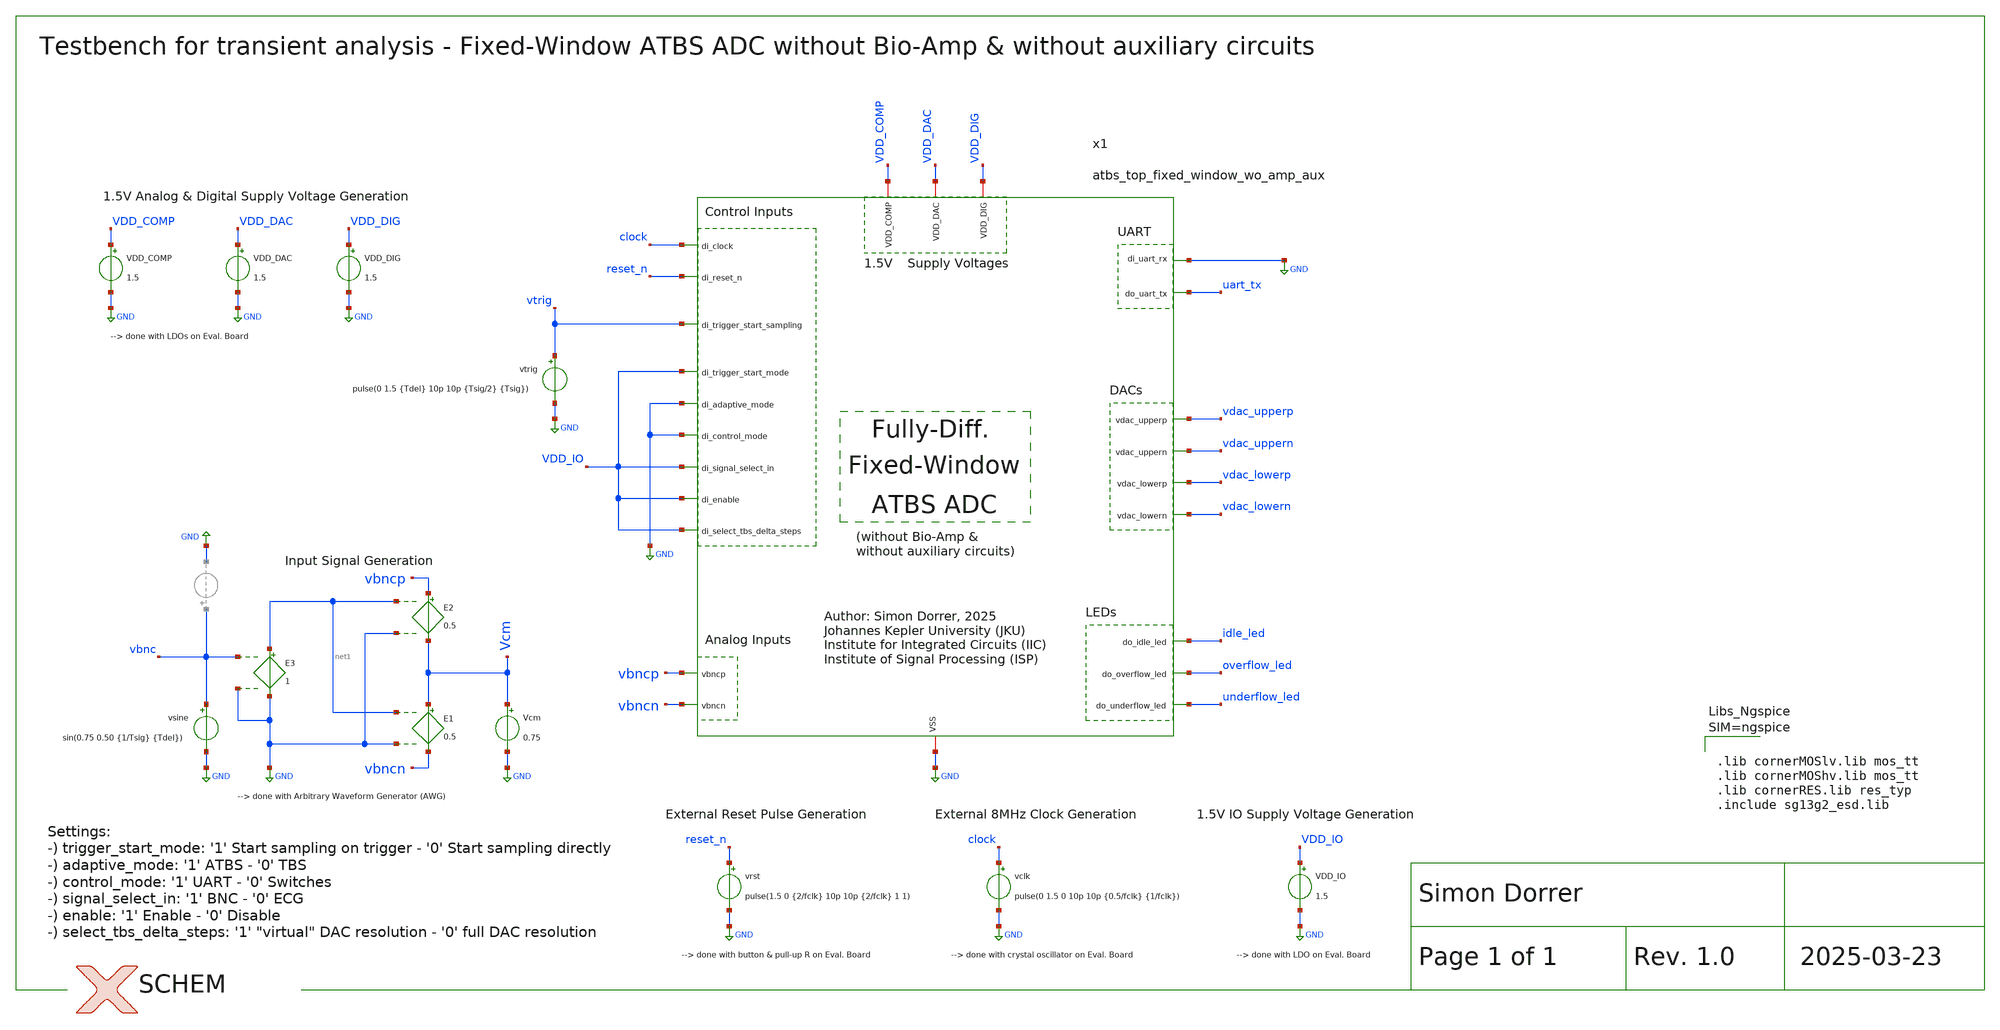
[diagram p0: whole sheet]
** sch_path: SG13G2_ATBS-ADC-main/xschem/top_level/testbenches/atbs_top_fixed_window_wo_amp_aux_tb_tran.sch
**.subckt atbs_top_fixed_window_wo_amp_aux_tb_tran
VDD_DAC VDD_DAC GND 1.5
VDD_COMP VDD_COMP GND 1.5
VDD_DIG VDD_DIG GND 1.5
VDD_IO VDD_IO GND 1.5
Vcm Vcm GND 0.75
E1 Vcm vbncn net1 GND 0.5
E2 vbncp Vcm net1 GND 0.5
E3 net1 GND vbnc GND 1
vsine vbnc GND sin(0.75 0.50 {1/Tsig} {Tdel})
vtrig vtrig GND pulse(0 1.5 {Tdel} 10p 10p {Tsig/2} {Tsig})
vrst reset_n GND pulse(1.5 0 {2/fclk} 10p 10p {2/fclk} 1 1)
vclk clock GND pulse(0 1.5 0 10p 10p {0.5/fclk} {1/fclk})
x1 VDD_DIG VDD_COMP clock reset_n vtrig VDD_DAC VDD_IO GND GND VDD_IO VDD_IO VDD_IO GND uart_tx
+ idle_led overflow_led underflow_led GND vbncp vbncn vdac_uppern vdac_lowern vdac_upperp vdac_lowerp
+ atbs_top_fixed_window_wo_amp_aux
**** begin user architecture code



* Gate-Level Analog Mixed Signal Simulation (.xspice)
.include /foss/designs/SG13G2_ATBS-ADC-main/xspice/atbs_core_fixed_window_board/atbs_core_fixed_window_board.xspice
.param temp=27
.param fclk=8000000
.csparam fclk=fclk
*.param Tsig=20m
*.param Tdel=20m
.param Tsig=200u
.param Tdel=100u
.csparam Tdel=Tdel
.csparam Tsig=Tsig
.options savecurrents method=gear reltol=1e-2 abstol=1e-12 gmin=1e-12 rshunt=1e12
.control

optran 0 0 0 1u 1m 0

* save all
save vbnc vbncp vbncn vtrig clock reset_n uart_tx idle_led overflow_led underflow_led vdac_upperp
+ vdac_uppern vdac_lowerp vdac_lowern
save x1.Vcm
save x1.spike x1.bio_amp_en x1.en_cap_1 x1.en_cap_2 x1.en_cap_3 x1.spdt_ctrl
save x1.phi_vcm_generator_1 x1.phi_vcm_generator_2 x1.phi_bias_1 x1.phi_bias_2 x1.phi_cmfb_1
+ x1.phi_cmfb_2 x1.phi_R_1 x1.phi_R_2
save x1.phi_comp x1.vcomp_upper x1.vcomp_lower x1.phi_dac_upper x1.dac_D0_upper x1.dac_D1_upper
+ x1.dac_D2_upper x1.dac_D3_upper x1.phi_dac_lower x1.dac_D0_lower x1.dac_D1_lower x1.dac_D2_lower x1.dac_D3_lower

* Transient Analysis
let tstep = 1/fclk
let tstop = Tdel + 4*Tsig
tran $&tstep $&tstop
write atbs_top_fixed_window_wo_amp_aux_tb_tran.raw

* Plotting Data
let vdac_upper = vdac_upperp - vdac_uppern
let vdac_lower = vdac_lowerp - vdac_lowern
plot v(vbnc) v(vtrig) v(vdac_upper) v(vdac_lower)

* Calculate Energy / Conversion (ToDo for all VDDs and add together in the end)
* i_int in As
* energy_conv in Ws = J
* let N = 1
* let t_conv = 1/fclk
* meas tran i_int INTEG i(VDD) from=0p to=t_conv
* let energy_conv = 1.5 * i_int / N

* let energy_conv_pico = energy_conv * 1e12
* echo Energy / Conversion $&energy_conv_pico pJ/conv

* Calculate Power Consumption (ToDo)
* let power = energy_conv / t_conv * 1e6
* echo Power Consumption $&power uW

* Writing Data
set wr_singlescale
set wr_vecnames
wrdata
+ /foss/designs/SG13G2_ATBS-ADC-main/python/plot_simulations/data/atbs_top_fixed_window_wo_amp_aux_tb_tran.txt v(vbnc) v(vtrig) v(vdac_upper) v(vdac_lower)

let uart_tx = uart_tx
wrdata
+ /foss/designs/SG13G2_ATBS-ADC-main/python/reconstruction/data/atbs_top_fixed_window_wo_amp_aux_tb_tran_uart.txt v(clock) v(uart_tx)
set appendwrite

.endc





.lib cornerMOSlv.lib mos_tt
.lib cornerMOShv.lib mos_tt
.lib cornerRES.lib res_typ
.include sg13g2_esd.lib



**** end user architecture code
**.ends

* expanding   symbol:  top_level/atbs_top_fixed_window_wo_amp_aux.sym # of pins=24
** sym_path: SG13G2_ATBS-ADC-main/xschem/top_level/atbs_top_fixed_window_wo_amp_aux.sym
** sch_path: SG13G2_ATBS-ADC-main/xschem/top_level/atbs_top_fixed_window_wo_amp_aux.sch
.subckt atbs_top_fixed_window_wo_amp_aux VDD_DIG VDD_COMP di_clock di_reset_n
+ di_trigger_start_sampling VDD_DAC di_trigger_start_mode di_adaptive_mode di_control_mode di_signal_select_in di_enable
+ di_select_tbs_delta_steps di_uart_rx do_uart_tx do_idle_led do_overflow_led do_underflow_led VSS vbncp vbncn vdac_uppern
+ vdac_lowern vdac_upperp vdac_lowerp
*.iopin VDD_DIG
*.iopin VDD_COMP
*.iopin VSS
*.ipin di_clock
*.ipin di_reset_n
*.iopin VDD_DAC
*.ipin di_uart_rx
*.opin do_uart_tx
*.ipin di_trigger_start_sampling
*.ipin di_trigger_start_mode
*.ipin di_adaptive_mode
*.ipin di_control_mode
*.ipin di_signal_select_in
*.ipin di_enable
*.ipin di_select_tbs_delta_steps
*.opin do_idle_led
*.opin do_overflow_led
*.opin do_underflow_led
*.ipin vbncp
*.ipin vbncn
*.opin vdac_upperp
*.opin vdac_lowern
*.opin vdac_uppern
*.opin vdac_lowerp
x4 VDD_COMP vdac_upperp vcomp_upper vdac_uppern phi_comp VSS DT_comparator
x5 VDD_COMP vdac_lowerp vcomp_lower vdac_lowern phi_comp VSS DT_comparator
x30 VDD_DIG VSS di_adaptive_mode bio_amp_en di_clock vcomp_lower vcomp_upper di_control_mode
+ dac_D0_lower dac_D1_lower dac_D2_lower dac_D3_lower dac_D0_upper dac_D1_upper dac_D2_upper dac_D3_upper
+ di_enable do_idle_led do_overflow_led phi_bias_1 phi_bias_2 phi_cmfb_1 phi_cmfb_2 phi_comp phi_dac_lower
+ phi_dac_upper phi_R_1 phi_R_2 phi_vcm_generator_1 phi_vcm_generator_2 di_reset_n en_cap_1 en_cap_2 en_cap_3
+ spdt_ctrl di_select_tbs_delta_steps di_signal_select_in spike di_trigger_start_mode di_trigger_start_sampling
+ di_uart_rx do_uart_tx do_underflow_led atbs_core_fixed_window_board
x32 VDD_DIG phi_vcm_generator_2 phi_vcm_generator_1 Vcm VSS vcm_generator C_VCM=1p W_P_VCM=1.0u
+ L_P_VCM=0.13u W_N_VCM=1.0u L_N_VCM=0.13u
x31 VDD_DAC vbncp vdac_upperp vdac_uppern vbncn dac_D0_lower dac_D1_lower dac_D2_lower dac_D3_lower
+ VSS VDD_DAC Vcm vdac_lowerp vdac_lowern phi_dac_lower dac_D0_upper dac_D1_upper dac_D2_upper
+ dac_D3_upper phi_dac_upper dac W_P_SPDT=1.0u L_P_SPDT=0.13u W_N_SPDT=1.0u L_N_SPDT=0.13u C2=1024f Cu=8f
+ Cucomp=8.1f
.ends


* expanding   symbol:  comparator/discrete_time/DT_comparator.sym # of pins=6
** sym_path: SG13G2_ATBS-ADC-main/xschem/comparator/discrete_time/DT_comparator.sym
** sch_path: SG13G2_ATBS-ADC-main/xschem/comparator/discrete_time/DT_comparator.sch
.subckt DT_comparator VDD vinp vout vinn di_clk VSS
*.iopin VDD
*.opin vout
*.iopin VSS
*.ipin vinp
*.ipin vinn
*.ipin di_clk
x2 VDD voutp_comp voutp_buf VSS buffer_lv W_P_INV=1.0u L_P_INV=0.13u W_N_INV=1.0u L_N_INV=0.13u
x3 VDD voutn_comp voutn_buf VSS buffer_lv W_P_INV=1.0u L_P_INV=0.13u W_N_INV=1.0u L_N_INV=0.13u
x5 VDD di_clk net1 VSS inverter_lv W_P=1.0u L_P=0.13u W_N=1.0u L_N=0.13u
* noconn #net2
x4 VDD voutp_buf net2 VSS vout voutn_buf SR_latch W_P_SR=1.0u L_P_SR=0.13u W_N_SR=1.0u L_N_SR=0.13u
x1 net1 di_clk VDD voutp_comp vinp VSS voutn_comp vinn dynamic_biasing_comparator
.ends


* expanding   symbol:  vcm_generator/vcm_generator.sym # of pins=5
** sym_path: SG13G2_ATBS-ADC-main/xschem/vcm_generator/vcm_generator.sym
** sch_path: SG13G2_ATBS-ADC-main/xschem/vcm_generator/vcm_generator.sch
.subckt vcm_generator VDD di_phi_2 di_phi_1 Vcm VSS  C_VCM=1p W_P_VCM=1.0u L_P_VCM=0.13u
+ W_N_VCM=1.0u L_N_VCM=0.13u
*.iopin VDD
*.opin Vcm
*.iopin VSS
*.ipin di_phi_1
*.ipin di_phi_2
x1 VDD di_phi_2 VSS net1 VDD di_phi_2_n transmission_gate_lv_wo_dummy W_P=W_P_VCM L_P=L_P_VCM
+ W_N=W_N_VCM L_N=L_N_VCM
x2 VDD di_phi_1 VSS Vcm net1 di_phi_1_n transmission_gate_lv_wo_dummy W_P=W_P_VCM L_P=L_P_VCM
+ W_N=W_N_VCM L_N=L_N_VCM
x3 VDD di_phi_2 VSS net3 net2 di_phi_2_n transmission_gate_lv_wo_dummy W_P=W_P_VCM L_P=L_P_VCM
+ W_N=W_N_VCM L_N=L_N_VCM
x4 VDD di_phi_1 VSS Vcm net3 di_phi_1_n transmission_gate_lv_wo_dummy W_P=W_P_VCM L_P=L_P_VCM
+ W_N=W_N_VCM L_N=L_N_VCM
x5 VDD di_phi_1 VSS VSS net2 di_phi_1_n transmission_gate_lv_wo_dummy W_P=W_P_VCM L_P=L_P_VCM
+ W_N=W_N_VCM L_N=L_N_VCM
x9 VDD di_phi_1 di_phi_1_n VSS inverter_lv W_P=W_P_VCM L_P=L_P_VCM W_N=W_N_VCM L_N=L_N_VCM
x8 VDD di_phi_2 di_phi_2_n VSS inverter_lv W_P=W_P_VCM L_P=L_P_VCM W_N=W_N_VCM L_N=L_N_VCM
C1 net1 net2 C_VCM m=1
C2 net3 VSS C_VCM m=1
.ends


* expanding   symbol:  dac/dac.sym # of pins=20
** sym_path: SG13G2_ATBS-ADC-main/xschem/dac/dac.sym
** sch_path: SG13G2_ATBS-ADC-main/xschem/dac/dac.sch
.subckt dac VDD vinp voutp1 voutn1 vinn di_D0_2 di_D1_2 di_D2_2 di_D3_2 VSS Vref Vcm voutp2 voutn2
+ di_clk_2 di_D0_1 di_D1_1 di_D2_1 di_D3_1 di_clk_1  W_P_SPDT=1.0u L_P_SPDT=0.13u W_N_SPDT=1.0u L_N_SPDT=0.13u
+ C2=1024f Cu=8f Cucomp=8.1f
*.opin voutp1
*.ipin di_D0_1
*.iopin VSS
*.iopin Vref
*.opin voutn1
*.ipin vinp
*.ipin vinn
*.ipin di_D1_1
*.ipin di_D2_1
*.ipin di_D3_1
*.opin voutp2
*.opin voutn2
*.iopin VDD
*.ipin Vcm
*.ipin di_clk_1
*.ipin di_D3_2
*.ipin di_D2_2
*.ipin di_D1_2
*.ipin di_D0_2
*.ipin di_clk_2
C2a vinp voutp1 C2 m=1
C2b vinn voutn1 C2 m=1
C1a net3 voutp1 Cucomp m=1
C1b net1 voutn1 Cucomp m=1
x2 VDD di_clk_1 VSS voutp1 Vcm clk_1_n transmission_gate_lv_wo_dummy W_P=1.0u L_P=0.13u W_N=1.0u
+ L_N=0.13u
x3 VDD di_clk_1 VSS voutn1 Vcm clk_1_n transmission_gate_lv_wo_dummy W_P=1.0u L_P=0.13u W_N=1.0u
+ L_N=0.13u
x1 VDD di_clk_1 clk_1_n VSS inverter_lv W_P=W_P_SPDT L_P=L_P_SPDT W_N=W_N_SPDT L_N=L_N_SPDT
x5 Vref VSS VSS di_D1_1 di_clk_1 VDD voutp1 unit_cell W_P_SPDT=W_P_SPDT L_P_SPDT=L_P_SPDT
+ W_N_SPDT=W_N_SPDT L_N_SPDT=L_N_SPDT Cu=2*Cu
x6 Vref VSS VSS di_D2_1 di_clk_1 VDD voutp1 unit_cell W_P_SPDT=W_P_SPDT L_P_SPDT=L_P_SPDT
+ W_N_SPDT=W_N_SPDT L_N_SPDT=L_N_SPDT Cu=4*Cu
x4 Vref VSS VSS di_D0_1 di_clk_1 VDD voutp1 unit_cell W_P_SPDT=W_P_SPDT L_P_SPDT=L_P_SPDT
+ W_N_SPDT=W_N_SPDT L_N_SPDT=L_N_SPDT Cu=Cu
x7 Vref VSS VSS di_D3_1 di_clk_1 VDD voutp1 unit_cell W_P_SPDT=W_P_SPDT L_P_SPDT=L_P_SPDT
+ W_N_SPDT=W_N_SPDT L_N_SPDT=L_N_SPDT Cu=8*Cu
x9 VSS Vref VSS di_D0_1 di_clk_1 VDD voutn1 unit_cell W_P_SPDT=W_P_SPDT L_P_SPDT=L_P_SPDT
+ W_N_SPDT=W_N_SPDT L_N_SPDT=L_N_SPDT Cu=Cu
x10 VSS Vref VSS di_D1_1 di_clk_1 VDD voutn1 unit_cell W_P_SPDT=W_P_SPDT L_P_SPDT=L_P_SPDT
+ W_N_SPDT=W_N_SPDT L_N_SPDT=L_N_SPDT Cu=2*Cu
x11 VSS Vref VSS di_D2_1 di_clk_1 VDD voutn1 unit_cell W_P_SPDT=W_P_SPDT L_P_SPDT=L_P_SPDT
+ W_N_SPDT=W_N_SPDT L_N_SPDT=L_N_SPDT Cu=4*Cu
x12 VSS Vref VSS di_D3_1 di_clk_1 VDD voutn1 unit_cell W_P_SPDT=W_P_SPDT L_P_SPDT=L_P_SPDT
+ W_N_SPDT=W_N_SPDT L_N_SPDT=L_N_SPDT Cu=8*Cu
C1 vinn voutp2 C2 m=1
C2 vinp voutn2 C2 m=1
C1c net2 voutp2 Cucomp m=1
C1d net4 voutn2 Cucomp m=1
x14 VDD di_clk_2 VSS voutp2 Vcm clk_2_n transmission_gate_lv_wo_dummy W_P=1.0u L_P=0.13u W_N=1.0u
+ L_N=0.13u
x15 VDD di_clk_2 VSS voutn2 Vcm clk_2_n transmission_gate_lv_wo_dummy W_P=1.0u L_P=0.13u W_N=1.0u
+ L_N=0.13u
x17 Vref VSS VSS di_D1_2 di_clk_2 VDD voutp2 unit_cell W_P_SPDT=W_P_SPDT L_P_SPDT=L_P_SPDT
+ W_N_SPDT=W_N_SPDT L_N_SPDT=L_N_SPDT Cu=2*Cu
x18 Vref VSS VSS di_D2_2 di_clk_2 VDD voutp2 unit_cell W_P_SPDT=W_P_SPDT L_P_SPDT=L_P_SPDT
+ W_N_SPDT=W_N_SPDT L_N_SPDT=L_N_SPDT Cu=4*Cu
x16 Vref VSS VSS di_D0_2 di_clk_2 VDD voutp2 unit_cell W_P_SPDT=W_P_SPDT L_P_SPDT=L_P_SPDT
+ W_N_SPDT=W_N_SPDT L_N_SPDT=L_N_SPDT Cu=Cu
x19 Vref VSS VSS di_D3_2 di_clk_2 VDD voutp2 unit_cell W_P_SPDT=W_P_SPDT L_P_SPDT=L_P_SPDT
+ W_N_SPDT=W_N_SPDT L_N_SPDT=L_N_SPDT Cu=8*Cu
x21 VSS Vref VSS di_D0_2 di_clk_2 VDD voutn2 unit_cell W_P_SPDT=W_P_SPDT L_P_SPDT=L_P_SPDT
+ W_N_SPDT=W_N_SPDT L_N_SPDT=L_N_SPDT Cu=Cu
x22 VSS Vref VSS di_D1_2 di_clk_2 VDD voutn2 unit_cell W_P_SPDT=W_P_SPDT L_P_SPDT=L_P_SPDT
+ W_N_SPDT=W_N_SPDT L_N_SPDT=L_N_SPDT Cu=2*Cu
x23 VSS Vref VSS di_D2_2 di_clk_2 VDD voutn2 unit_cell W_P_SPDT=W_P_SPDT L_P_SPDT=L_P_SPDT
+ W_N_SPDT=W_N_SPDT L_N_SPDT=L_N_SPDT Cu=4*Cu
x24 VSS Vref VSS di_D3_2 di_clk_2 VDD voutn2 unit_cell W_P_SPDT=W_P_SPDT L_P_SPDT=L_P_SPDT
+ W_N_SPDT=W_N_SPDT L_N_SPDT=L_N_SPDT Cu=8*Cu
x8 VDD di_clk_1 VSS net3 VSS Vref spdt_switch W_P_TG=W_P_SPDT L_P_TG=L_P_SPDT W_N_TG=W_N_SPDT
+ L_N_TG=L_N_SPDT
x13 VDD di_clk_1 VSS net1 Vref VSS spdt_switch W_P_TG=W_P_SPDT L_P_TG=L_P_SPDT W_N_TG=W_N_SPDT
+ L_N_TG=L_N_SPDT
x20 VDD di_clk_2 VSS net2 VSS Vref spdt_switch W_P_TG=W_P_SPDT L_P_TG=L_P_SPDT W_N_TG=W_N_SPDT
+ L_N_TG=L_N_SPDT
x25 VDD di_clk_2 VSS net4 Vref VSS spdt_switch W_P_TG=W_P_SPDT L_P_TG=L_P_SPDT W_N_TG=W_N_SPDT
+ L_N_TG=L_N_SPDT
x26 VDD di_clk_2 clk_2_n VSS inverter_lv W_P=W_P_SPDT L_P=L_P_SPDT W_N=W_N_SPDT L_N=L_N_SPDT
.ends


* expanding   symbol:  buffer/buffer_lv.sym # of pins=4
** sym_path: SG13G2_ATBS-ADC-main/xschem/buffer/buffer_lv.sym
** sch_path: SG13G2_ATBS-ADC-main/xschem/buffer/buffer_lv.sch
.subckt buffer_lv VDD vin vout VSS  W_P_INV=3.0u L_P_INV=0.13u W_N_INV=1.0u L_N_INV=0.13u
*.ipin vin
*.iopin VDD
*.iopin VSS
*.opin vout
x1 VDD vin net1 VSS inverter_lv W_P=W_P_INV L_P=L_P_INV W_N=W_N_INV L_N=L_N_INV
x2 VDD net1 vout VSS inverter_lv W_P=W_P_INV L_P=L_P_INV W_N=W_N_INV L_N=L_N_INV
.ends


* expanding   symbol:  inverter/inverter_lv.sym # of pins=4
** sym_path: SG13G2_ATBS-ADC-main/xschem/inverter/inverter_lv.sym
** sch_path: SG13G2_ATBS-ADC-main/xschem/inverter/inverter_lv.sch
.subckt inverter_lv VDD vin vout VSS  W_P=3.0u L_P=0.13u W_N=1.0u L_N=0.13u
*.ipin vin
*.iopin VDD
*.iopin VSS
*.opin vout
XM1 vout vin VDD VDD sg13_lv_pmos w=W_P l=L_P ng=1 m=1 mm_ok=1
XM2 vout vin VSS VSS sg13_lv_nmos w=W_N l=L_N ng=1 m=1 mm_ok=1
.ends


* expanding   symbol:  comparator/SR_latch/SR_latch.sym # of pins=6
** sym_path: SG13G2_ATBS-ADC-main/xschem/comparator/SR_latch/SR_latch.sym
** sch_path: SG13G2_ATBS-ADC-main/xschem/comparator/SR_latch/SR_latch.sch
.subckt SR_latch VDD S Qn VSS Q R  W_P_SR=1.0u L_P_SR=0.13u W_N_SR=1.0u L_N_SR=0.13u
*.iopin VDD
*.opin Q
*.iopin VSS
*.ipin S
*.ipin R
*.opin Qn
x1 VDD Q R Qn VSS NOR_gate W_P=W_P_SR L_P=L_P_SR W_N=W_N_SR L_N=L_N_SR
x2 VDD Qn Q S VSS NOR_gate W_P=W_P_SR L_P=L_P_SR W_N=W_N_SR L_N=L_N_SR
.ends


* expanding   symbol:  comparator/discrete_time/Dynamic-biasing/dynamic_biasing_comparator.sym # of
*+ pins=8
** sym_path: SG13G2_ATBS-ADC-main/xschem/comparator/discrete_time/Dynamic-biasing/dynamic_biasing_comparator.sym
** sch_path: SG13G2_ATBS-ADC-main/xschem/comparator/discrete_time/Dynamic-biasing/dynamic_biasing_comparator.sch
.subckt dynamic_biasing_comparator di_clk_n di_clk VDD voutp vinp VSS voutn vinn
*.iopin VDD
*.opin voutp
*.opin voutn
*.ipin di_clk_n
*.iopin VSS
*.ipin vinp
*.ipin vinn
*.ipin di_clk
XM3a vs di_clk vctail VSS sg13_lv_nmos w=1.0u l=0.13u ng=1 m=1 mm_ok=1
XM12 voutp di_clk_n VSS VSS sg13_lv_nmos w=1.0u l=0.13u ng=1 m=1 mm_ok=1
XM8 net1 voutn VDD VDD sg13_lv_pmos w=2.0u l=0.13u ng=2 m=1 mm_ok=1
XM10 voutp voutn VSS VSS sg13_lv_nmos w=1.0u l=0.13u ng=1 m=1 mm_ok=1
XM11 voutn voutp VSS VSS sg13_lv_nmos w=1.0u l=0.13u ng=1 m=1 mm_ok=1
XM13 voutn di_clk_n VSS VSS sg13_lv_nmos w=1.0u l=0.13u ng=1 m=1 mm_ok=1
CPn vcpn VSS 300f m=1
CPp vcpp VSS 300f m=1
XM9 net2 voutp VDD VDD sg13_lv_pmos w=2.0u l=0.13u ng=2 m=1 mm_ok=1
XM6 voutp vcpn net1 VDD sg13_lv_pmos w=2.0u l=0.13u ng=2 m=1 mm_ok=1
XM7 voutn vcpp net2 VDD sg13_lv_pmos w=2.0u l=0.13u ng=2 m=1 mm_ok=1
CTAIL vctail VSS 600f m=1
XM3b vctail di_clk_n VSS VSS sg13_lv_nmos w=1.0u l=0.13u ng=1 m=1 mm_ok=1
XM1 vcpn vinp vs VSS sg13_lv_nmos w=1.0u l=0.13u ng=1 m=1 mm_ok=1
XM2 vcpp vinn vs VSS sg13_lv_nmos w=1.0u l=0.13u ng=1 m=1 mm_ok=1
XM4 vcpn di_clk VDD VDD sg13_lv_pmos w=1.0u l=0.13u ng=1 m=1 mm_ok=1
XM5 vcpp di_clk VDD VDD sg13_lv_pmos w=1.0u l=0.13u ng=1 m=1 mm_ok=1
.ends


* expanding   symbol:  transmission_gate/transmission_gate_lv_wo_dummy.sym # of pins=6
** sym_path: SG13G2_ATBS-ADC-main/xschem/transmission_gate/transmission_gate_lv_wo_dummy.sym
** sch_path: SG13G2_ATBS-ADC-main/xschem/transmission_gate/transmission_gate_lv_wo_dummy.sch
.subckt transmission_gate_lv_wo_dummy VDD di_tg_ctrl VSS v_b v_a di_tg_ctrl_n  W_P=1.0u L_P=0.13u
+ W_N=1.0u L_N=0.13u
*.iopin v_a
*.iopin v_b
*.iopin VDD
*.iopin VSS
*.ipin di_tg_ctrl
*.ipin di_tg_ctrl_n
XM1 v_a di_tg_ctrl v_b VSS sg13_lv_nmos w=W_N l=L_N ng=1 m=1 mm_ok=1
XM2 v_a di_tg_ctrl_n v_b VDD sg13_lv_pmos w=W_P l=L_P ng=1 m=1 mm_ok=1
.ends


* expanding   symbol:  dac/unit_cell.sym # of pins=7
** sym_path: SG13G2_ATBS-ADC-main/xschem/dac/unit_cell.sym
** sch_path: SG13G2_ATBS-ADC-main/xschem/dac/unit_cell.sch
.subckt unit_cell v1 v0 VSS di_cell_en di_clk VDD vtop  W_P_SPDT=1.0u L_P_SPDT=0.13u W_N_SPDT=1.0u
+ L_N_SPDT=0.13u Cu=8f
*.ipin di_cell_en
*.iopin VSS
*.iopin v0
*.iopin VDD
*.ipin di_clk
*.iopin v1
*.iopin vtop
x1 VDD di_clk VSS net1 v0 v1 di_cell_en_n spdt_hz_switch W_P_TG=W_P_SPDT L_P_TG=L_P_SPDT
+ W_N_TG=W_N_SPDT L_N_TG=L_N_SPDT
C1 net1 vtop Cu m=1
x3 VDD di_cell_en di_cell_en_n VSS inverter_lv W_P=W_P_SPDT L_P=W_P_SPDT W_N=W_N_SPDT L_N=W_N_SPDT
.ends


* expanding   symbol:  spdt_switch/spdt_switch.sym # of pins=6
** sym_path: SG13G2_ATBS-ADC-main/xschem/spdt_switch/spdt_switch.sym
** sch_path: SG13G2_ATBS-ADC-main/xschem/spdt_switch/spdt_switch.sch
.subckt spdt_switch VDD di_spdt_ctrl VSS v_c v_b v_a  W_P_TG=3.0u L_P_TG=0.13u W_N_TG=1.0u
+ L_N_TG=0.13u
*.iopin v_a
*.iopin v_b
*.iopin v_c
*.iopin VDD
*.iopin VSS
*.ipin di_spdt_ctrl
x1 VDD di_spdt_ctrl VSS v_c v_a di_spdt_ctrl_n transmission_gate_lv_wo_dummy W_P=W_P_TG L_P=L_P_TG
+ W_N=W_N_TG L_N=L_N_TG
x2 VDD di_spdt_ctrl_n VSS v_b v_c di_spdt_ctrl transmission_gate_lv_wo_dummy W_P=W_P_TG L_P=L_P_TG
+ W_N=W_N_TG L_N=L_N_TG
x8 VDD di_spdt_ctrl di_spdt_ctrl_n VSS inverter_lv W_P=W_P_TG L_P=L_P_TG W_N=W_N_TG L_N=L_N_TG
.ends


* expanding   symbol:  comparator/NOR_gate/NOR_gate.sym # of pins=5
** sym_path: SG13G2_ATBS-ADC-main/xschem/comparator/NOR_gate/NOR_gate.sym
** sch_path: SG13G2_ATBS-ADC-main/xschem/comparator/NOR_gate/NOR_gate.sch
.subckt NOR_gate VDD C A B VSS  W_P=1.0u L_P=0.13u W_N=0.5u L_N=0.13u
*.iopin VDD
*.opin C
*.iopin VSS
*.ipin A
*.ipin B
XM1 C A VSS VSS sg13_lv_nmos w=W_N l=L_N ng=1 m=1 mm_ok=1
XM2 C B VSS VSS sg13_lv_nmos w=W_N l=L_N ng=1 m=1 mm_ok=1
XM3 C B net1 VDD sg13_lv_pmos w=W_P l=L_P ng=1 m=1 mm_ok=1
XM4 net1 A VDD VDD sg13_lv_pmos w=W_P l=L_P ng=1 m=1 mm_ok=1
XM5 C A net2 VDD sg13_lv_pmos w=W_P l=L_P ng=1 m=1 mm_ok=1
XM6 net2 B VDD VDD sg13_lv_pmos w=W_P l=L_P ng=1 m=1 mm_ok=1
.ends


* expanding   symbol:  spdt_switch/spdt_hz_switch.sym # of pins=7
** sym_path: SG13G2_ATBS-ADC-main/xschem/spdt_switch/spdt_hz_switch.sym
** sch_path: SG13G2_ATBS-ADC-main/xschem/spdt_switch/spdt_hz_switch.sch
.subckt spdt_hz_switch VDD di_spdt_ctrl VSS v_c v_b v_a di_spdt_hz  W_P_TG=3.0u L_P_TG=0.13u
+ W_N_TG=1.0u L_N_TG=0.13u
*.iopin v_a
*.iopin v_b
*.iopin v_c
*.iopin VDD
*.iopin VSS
*.ipin di_spdt_ctrl
*.ipin di_spdt_hz
x1 VDD di_spdt_ctrl VSS net1 v_a di_spdt_ctrl_n transmission_gate_lv_wo_dummy W_P=W_P_TG L_P=L_P_TG
+ W_N=W_N_TG L_N=L_N_TG
x2 VDD di_spdt_ctrl_n VSS v_b net1 di_spdt_ctrl transmission_gate_lv_wo_dummy W_P=W_P_TG L_P=L_P_TG
+ W_N=W_N_TG L_N=L_N_TG
x8 VDD di_spdt_ctrl di_spdt_ctrl_n VSS inverter_lv W_P=W_P_TG L_P=L_P_TG W_N=W_N_TG L_N=L_N_TG
x3 VDD di_spdt_hz di_spdt_hz_n VSS inverter_lv W_P=W_P_TG L_P=L_P_TG W_N=W_N_TG L_N=L_N_TG
x4 VDD di_spdt_hz_n VSS v_c net1 di_spdt_hz transmission_gate_lv_wo_dummy W_P=W_P_TG L_P=L_P_TG
+ W_N=W_N_TG L_N=L_N_TG
.ends

.GLOBAL GND
.end
